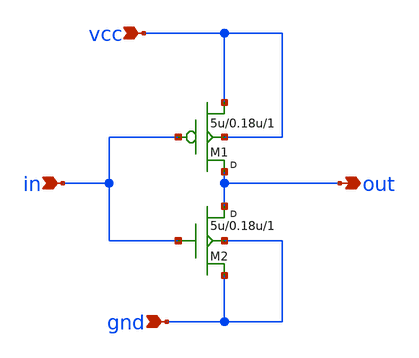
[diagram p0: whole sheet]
** sch_path: xschem/osu_soc_tsmc018/inverter/invx1.sch
**.subckt invx1 in out vcc gnd
*.ipin in
*.opin out
*.ipin vcc
*.ipin gnd
M1 out in vcc vcc pmos w=5u l=0.18u m=1
M2 out in gnd gnd nmos w=5u l=0.18u m=1
**.ends
.end
